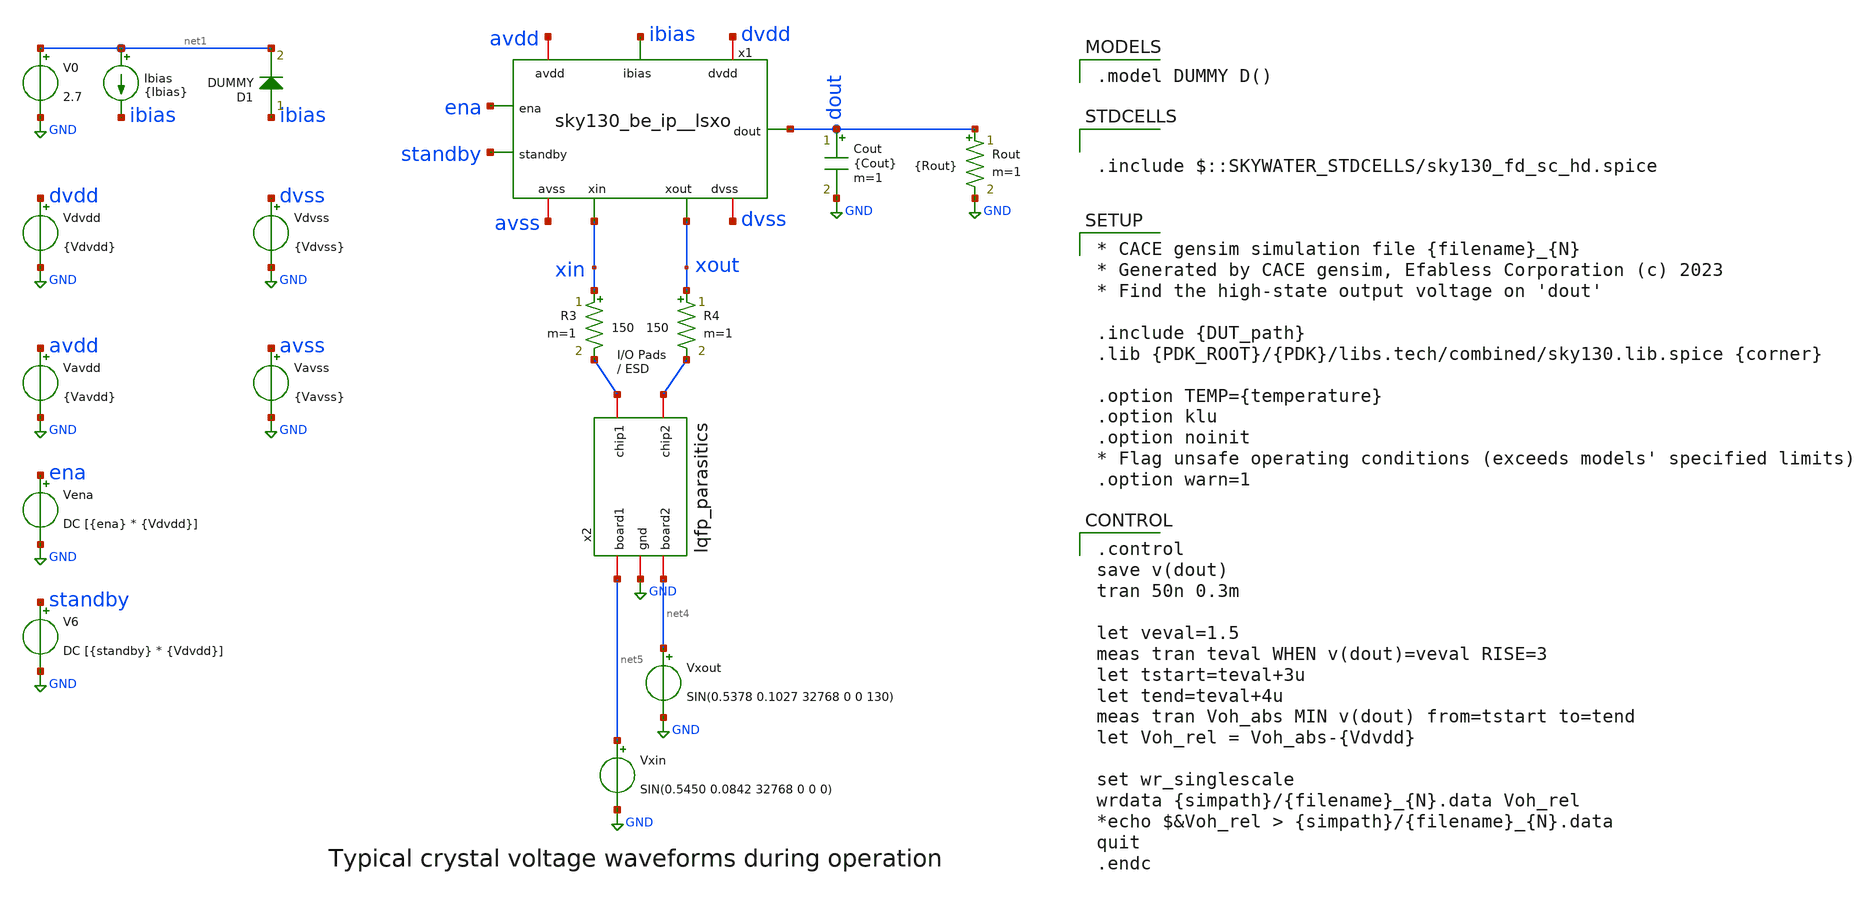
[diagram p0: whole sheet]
** sch_path: cace/tb_voh.sch

.include $::SKYWATER_STDCELLS/sky130_fd_sc_hd.spice

**.subckt tb_voh
Vdvdd dvdd GND {Vdvdd}
Vavdd avdd GND {Vavdd}
Ibias net1 ibias {Ibias}
Cout dout GND {Cout} m=1
V0 net1 GND 2.7
V6 standby GND DC [{standby} * {Vdvdd}]
R3 xin net2 150 m=1
R4 xout net3 150 m=1
x2 net3 net2 GND net5 net4 lqfp_parasitics
Vena ena GND DC [{ena} * {Vdvdd}]
D1 ibias net1 DUMMY area=100
x1 avdd avss dvdd dvss ibias ena standby dout xin xout sky130_be_ip__lsxo
Vdvss dvss GND {Vdvss}
Vavss avss GND {Vavss}
Rout dout GND {Rout} m=1
Vxout net4 GND SIN(0.5378 0.1027 32768 0 0 130)
Vxin net5 GND SIN(0.5450 0.0842 32768 0 0 0)
**** begin user architecture code

.model DUMMY D()


.control
save v(dout)
tran 50n 0.3m

let veval=1.5
meas tran teval WHEN v(dout)=veval RISE=3
let tstart=teval+3u
let tend=teval+4u
meas tran Voh_abs MIN v(dout) from=tstart to=tend
let Voh_rel = Voh_abs-{Vdvdd}

set wr_singlescale
wrdata {simpath}/{filename}_{N}.data Voh_rel
*echo $&Voh_rel > {simpath}/{filename}_{N}.data
quit
.endc



* CACE gensim simulation file {filename}_{N}
* Generated by CACE gensim, Efabless Corporation (c) 2023
* Find the high-state output voltage on 'dout'

.include {DUT_path}
.lib {PDK_ROOT}/{PDK}/libs.tech/combined/sky130.lib.spice {corner}

.option TEMP={temperature}
.option klu
.option noinit
* Flag unsafe operating conditions (exceeds models' specified limits)
.option warn=1


**** end user architecture code
**.ends
.GLOBAL GND
.end
